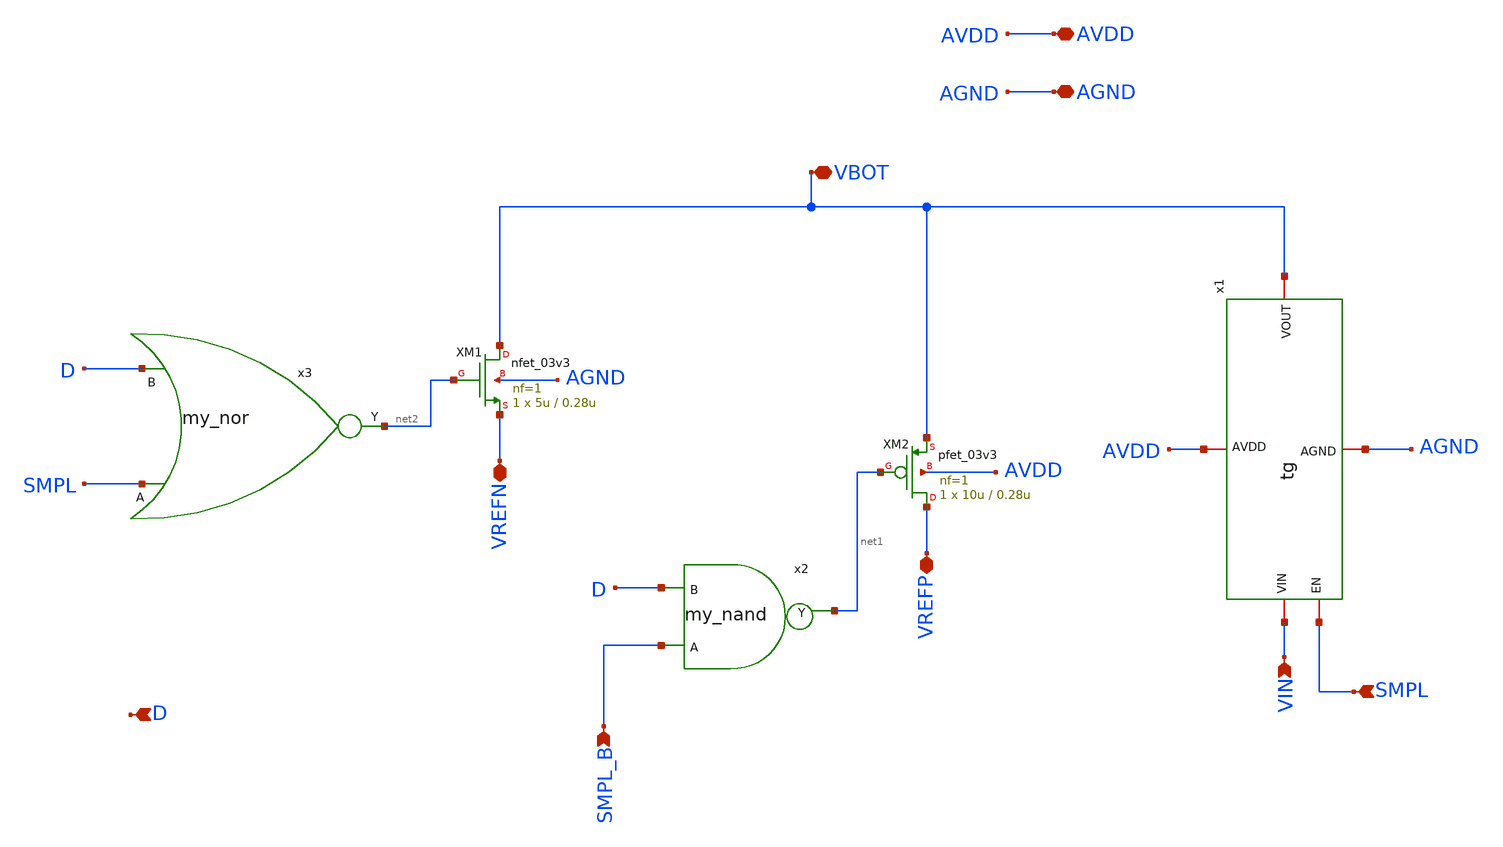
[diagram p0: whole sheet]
** sch_path: bot_plate_sw.sch
**.subckt bot_plate_sw AVDD AGND VIN SMPL VREFN VREFP D VBOT SMPL_B
*.iopin AVDD
*.iopin AGND
*.ipin VIN
*.ipin SMPL
*.iopin VREFN
*.iopin VREFP
*.ipin D
*.iopin VBOT
*.ipin SMPL_B
XM1 VBOT net2 VREFN AGND nfet_03v3 L=0.28u W=5u nf=1 ad='int((nf+1)/2) * W/nf * 0.18u' as='int((nf+2)/2) * W/nf * 0.18u'
+ pd='2*int((nf+1)/2) * (W/nf + 0.18u)' ps='2*int((nf+2)/2) * (W/nf + 0.18u)' nrd='0.18u / W' nrs='0.18u / W'
+ sa=0 sb=0 sd=0 m=1
XM2 VREFP net1 VBOT AVDD pfet_03v3 L=0.28u W=10u nf=1 ad='int((nf+1)/2) * W/nf * 0.18u' as='int((nf+2)/2) * W/nf * 0.18u'
+ pd='2*int((nf+1)/2) * (W/nf + 0.18u)' ps='2*int((nf+2)/2) * (W/nf + 0.18u)' nrd='0.18u / W' nrs='0.18u / W'
+ sa=0 sb=0 sd=0 m=1
x1 SMPL AGND VBOT VIN AVDD tg
x2 D net1 SMPL_B my_nand
x3 D net2 SMPL my_nor
**.ends

* expanding   symbol:  tg.sym # of pins=5
** sym_path: tg.sym
** sch_path: tg.sch
.subckt tg EN AGND VOUT VIN AVDD
*.iopin AGND
*.iopin AVDD
*.iopin EN
*.iopin VOUT
*.iopin VIN
XM1 VOUT EN VIN AGND nfet_03v3 L=0.28u W=5u nf=1 ad='int((nf+1)/2) * W/nf * 0.18u' as='int((nf+2)/2) * W/nf * 0.18u'
+ pd='2*int((nf+1)/2) * (W/nf + 0.18u)' ps='2*int((nf+2)/2) * (W/nf + 0.18u)' nrd='0.18u / W' nrs='0.18u / W'
+ sa=0 sb=0 sd=0 m=1
XM2 VOUT ENB VIN AVDD pfet_03v3 L=0.28u W=10u nf=1 ad='int((nf+1)/2) * W/nf * 0.18u' as='int((nf+2)/2) * W/nf * 0.18u'
+ pd='2*int((nf+1)/2) * (W/nf + 0.18u)' ps='2*int((nf+2)/2) * (W/nf + 0.18u)' nrd='0.18u / W' nrs='0.18u / W'
+ sa=0 sb=0 sd=0 m=1
E1 ENB AVDD EN AGND -1
.ends


* expanding   symbol:  my_nand.sym # of pins=3
** sym_path: my_nand.sym
** sch_path: my_nand.sch
.subckt my_nand B Y A
*.ipin B
*.ipin A
*.opin Y
**** begin user architecture code

a6 [A B] Yi nand1
.model nand1 d_nand(rise_delay = 1e-9 fall_delay = 1e-9 input_load = 1e-12)

v1 Yi Y 0


**** end user architecture code
.ends


* expanding   symbol:  my_nor.sym # of pins=3
** sym_path: my_nor.sym
** sch_path: my_nor.sch
.subckt my_nor B Y A
*.ipin B
*.ipin A
*.opin Y
**** begin user architecture code

a6 [A B] Yi nor1
.model nor1 d_nor(rise_delay = 1e-9 fall_delay = 1e-9 input_load = 1e-12)

v1 Yi Y 0


**** end user architecture code
.ends

.end
